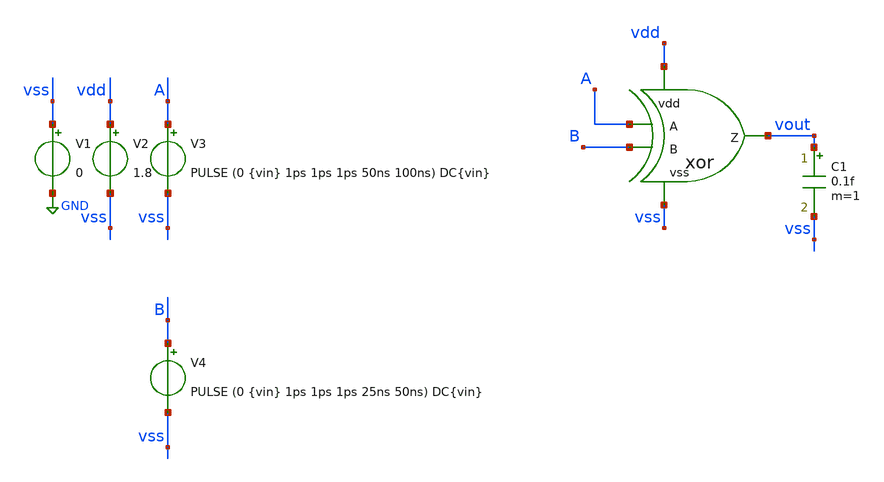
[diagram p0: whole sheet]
** sch_path: track_vlsi/lado/sch/tb_xor.sch
**.subckt tb_xor
V1 vss GND 0
V2 vdd vss 1.8
V3 A vss PULSE (0 {vin} 1ps 1ps 1ps 50ns 100ns) DC{vin}
C1 vout vss 0.1f m=1
V4 B vss PULSE (0 {vin} 1ps 1ps 1ps 25ns 50ns) DC{vin}
xor vdd A B vout vss xor
**** begin user architecture code



*parametros
.param vin=1.8
.options TEMP=27.0

*include

.lib /home/eamta/skywater/skywater-pdk/libraries/sky130_fd_pr_ngspice/latest/models/corners/sky130.lib TT

*signals to save
.save all
*+ @m.x1.xm2.msky130_fd_pr__nfet_01v8[id] @m.x1.xm2.msky130_fd_pr__nfet_01v8[gm]
*+ @m.x1.xm1.msky130_fd_pr__pfet_01v8[id] @m.x1.xm1.msky130_fd_pr__pfet_01v8[gm]




*config simulacion

.control
  tran 0.1ns 0.5us
  setplot tran1
  plot v(vout) v(A) v(B)
  write tb_inverter_trans.raw
  gnuplot salida v(A) v(B) v(vout)
  reset
  dc V3 0 1.8 0.01
  setplot dc1
  plot v(vout) v(A) v(B)
  write tb_inverter_dc.raw
  reset
  op
  print all

.endc

.end


**** end user architecture code
**.ends

* expanding   symbol:  /home/eamta/eamta2021/sch/xor/xor.sym # of pins=5
** sym_path: track_vlsi/lado/sch/xor.sym
** sch_path: track_vlsi/lado/sch/xor.sch
.subckt xor vdd A B Z vss
*.ipin A
*.ipin vss
*.ipin vdd
*.opin Z
*.ipin B
XM0 net1 Bb vdd vdd sky130_fd_pr__pfet_01v8 L=0.15 W=0.9 nf=1 ad='int((nf+1)/2) * W/nf * 0.29' as='int((nf+2)/2) * W/nf * 0.29'
+ pd='2*int((nf+1)/2) * (W/nf + 0.29)' ps='2*int((nf+2)/2) * (W/nf + 0.29)' nrd='0.29 / W' nrs='0.29 / W'
+ sa=0 sb=0 sd=0 mult=1 m=1
XM5 Z A net3 vss sky130_fd_pr__nfet_01v8 L=0.15 W=0.9 nf=1 ad='int((nf+1)/2) * W/nf * 0.29' as='int((nf+2)/2) * W/nf * 0.29'
+ pd='2*int((nf+1)/2) * (W/nf + 0.29)' ps='2*int((nf+2)/2) * (W/nf + 0.29)' nrd='0.29 / W' nrs='0.29 / W'
+ sa=0 sb=0 sd=0 mult=1 m=1
XM1 net1 Ab vdd vdd sky130_fd_pr__pfet_01v8 L=0.15 W=0.9 nf=1 ad='int((nf+1)/2) * W/nf * 0.29' as='int((nf+2)/2) * W/nf * 0.29'
+ pd='2*int((nf+1)/2) * (W/nf + 0.29)' ps='2*int((nf+2)/2) * (W/nf + 0.29)' nrd='0.29 / W' nrs='0.29 / W'
+ sa=0 sb=0 sd=0 mult=1 m=1
XM2 Z A net1 vdd sky130_fd_pr__pfet_01v8 L=0.15 W=0.9 nf=1 ad='int((nf+1)/2) * W/nf * 0.29' as='int((nf+2)/2) * W/nf * 0.29'
+ pd='2*int((nf+1)/2) * (W/nf + 0.29)' ps='2*int((nf+2)/2) * (W/nf + 0.29)' nrd='0.29 / W' nrs='0.29 / W'
+ sa=0 sb=0 sd=0 mult=1 m=1
XM4 Z Ab net2 vss sky130_fd_pr__nfet_01v8 L=0.15 W=0.9 nf=1 ad='int((nf+1)/2) * W/nf * 0.29' as='int((nf+2)/2) * W/nf * 0.29'
+ pd='2*int((nf+1)/2) * (W/nf + 0.29)' ps='2*int((nf+2)/2) * (W/nf + 0.29)' nrd='0.29 / W' nrs='0.29 / W'
+ sa=0 sb=0 sd=0 mult=1 m=1
XM6 net2 Bb vss vss sky130_fd_pr__nfet_01v8 L=0.15 W=0.9 nf=1 ad='int((nf+1)/2) * W/nf * 0.29' as='int((nf+2)/2) * W/nf * 0.29'
+ pd='2*int((nf+1)/2) * (W/nf + 0.29)' ps='2*int((nf+2)/2) * (W/nf + 0.29)' nrd='0.29 / W' nrs='0.29 / W'
+ sa=0 sb=0 sd=0 mult=1 m=1
XM8 Ab A vdd vdd sky130_fd_pr__pfet_01v8 L=0.15 W=0.9 nf=1 ad='int((nf+1)/2) * W/nf * 0.29' as='int((nf+2)/2) * W/nf * 0.29'
+ pd='2*int((nf+1)/2) * (W/nf + 0.29)' ps='2*int((nf+2)/2) * (W/nf + 0.29)' nrd='0.29 / W' nrs='0.29 / W'
+ sa=0 sb=0 sd=0 mult=1 m=1
XM9 Ab A vss vss sky130_fd_pr__nfet_01v8 L=0.15 W=0.45 nf=1 ad='int((nf+1)/2) * W/nf * 0.29' as='int((nf+2)/2) * W/nf * 0.29'
+ pd='2*int((nf+1)/2) * (W/nf + 0.29)' ps='2*int((nf+2)/2) * (W/nf + 0.29)' nrd='0.29 / W' nrs='0.29 / W'
+ sa=0 sb=0 sd=0 mult=1 m=1
XM3 Z B net1 vdd sky130_fd_pr__pfet_01v8 L=0.15 W=0.9 nf=1 ad='int((nf+1)/2) * W/nf * 0.29' as='int((nf+2)/2) * W/nf * 0.29'
+ pd='2*int((nf+1)/2) * (W/nf + 0.29)' ps='2*int((nf+2)/2) * (W/nf + 0.29)' nrd='0.29 / W' nrs='0.29 / W'
+ sa=0 sb=0 sd=0 mult=1 m=1
XM12 Bb B vss vss sky130_fd_pr__nfet_01v8 L=0.15 W=0.45 nf=1 ad='int((nf+1)/2) * W/nf * 0.29' as='int((nf+2)/2) * W/nf * 0.29'
+ pd='2*int((nf+1)/2) * (W/nf + 0.29)' ps='2*int((nf+2)/2) * (W/nf + 0.29)' nrd='0.29 / W' nrs='0.29 / W'
+ sa=0 sb=0 sd=0 mult=1 m=1
XM7 net3 B vss vss sky130_fd_pr__nfet_01v8 L=0.15 W=0.9 nf=1 ad='int((nf+1)/2) * W/nf * 0.29' as='int((nf+2)/2) * W/nf * 0.29'
+ pd='2*int((nf+1)/2) * (W/nf + 0.29)' ps='2*int((nf+2)/2) * (W/nf + 0.29)' nrd='0.29 / W' nrs='0.29 / W'
+ sa=0 sb=0 sd=0 mult=1 m=1
XM10 Bb B vdd vdd sky130_fd_pr__pfet_01v8 L=0.15 W=0.9 nf=1 ad='int((nf+1)/2) * W/nf * 0.29' as='int((nf+2)/2) * W/nf * 0.29'
+ pd='2*int((nf+1)/2) * (W/nf + 0.29)' ps='2*int((nf+2)/2) * (W/nf + 0.29)' nrd='0.29 / W' nrs='0.29 / W'
+ sa=0 sb=0 sd=0 mult=1 m=1
.ends

.GLOBAL GND
.end
